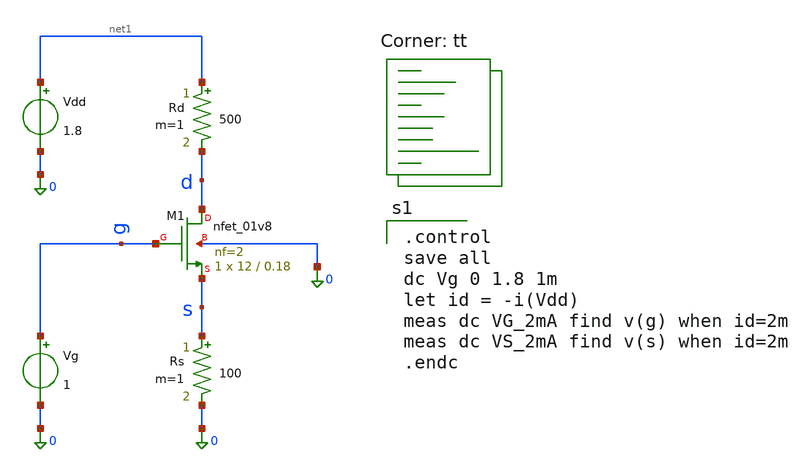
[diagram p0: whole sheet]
** sch_path: Homework 6 - Simulation on Open Source Softwares/Simulations/ex2_vgs.sch
**.subckt ex2_vgs
XM1 d g s 0 sky130_fd_pr__nfet_01v8 L=0.18 W=12 nf=2 ad='int((2 + 1)/2) * 12 / 2 * 0.29' as='int((2 + 2)/2) * 12 / 2 * 0.29'
+ pd='2*int((2 + 1)/2) * (12 / 2 + 0.29)' ps='2*int((2 + 2)/2) * (12 / 2 + 0.29)' nrd='0.29 / 12 ' nrs='0.29 / 12 '
+ sa=0 sb=0 sd=0 mult=1 m=1
Vg g 0 1
Rd net1 d 500 m=1
Rs s 0 100 m=1
Vdd net1 0 1.8
**** begin user architecture code
.lib $::SKYWATER_MODELS/sky130.lib.spice tt

.control
save all
dc Vg 0 1.8 1m
let id = -i(Vdd)
meas dc VG_2mA find v(g) when id=2m
meas dc VS_2mA find v(s) when id=2m
.endc

**** end user architecture code
**.ends
.end
